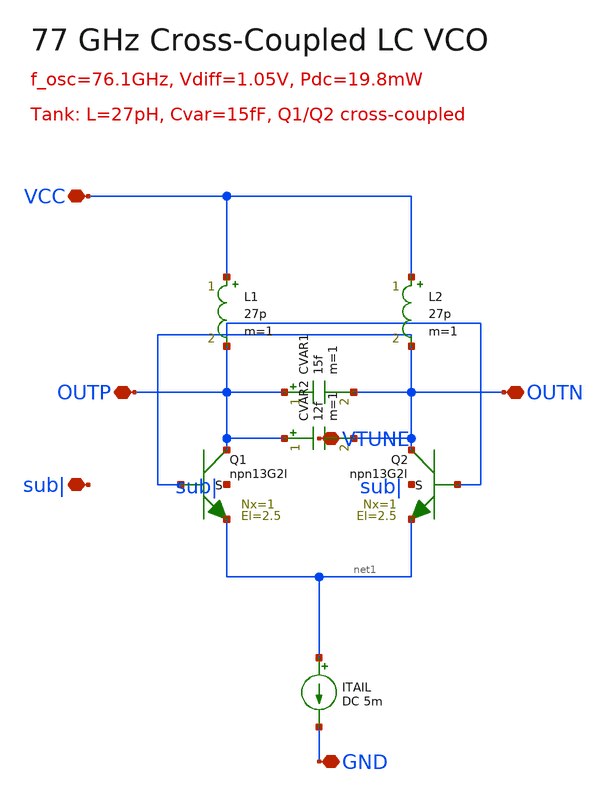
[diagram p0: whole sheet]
** sch_path: xschem/blocks/VCO_77G.sch
**.subckt VCO_77G VCC GND OUTP OUTN VTUNE sub|
*.iopin VCC
*.iopin GND
*.iopin OUTP
*.iopin OUTN
*.iopin VTUNE
*.iopin sub|
XQ1 OUTP OUTN net1 sub| npn13G2l Nx=1 El=2.5 mm_ok=1
XQ2 OUTN OUTP net1 sub| npn13G2l Nx=1 El=2.5 mm_ok=1
L1 VCC OUTP 27p m=1
L2 VCC OUTN 27p m=1
CVAR1 OUTP OUTN 15f m=1
CVAR2 OUTP OUTN 12f m=1
ITAIL net1 GND DC 5m
**.ends
.end
